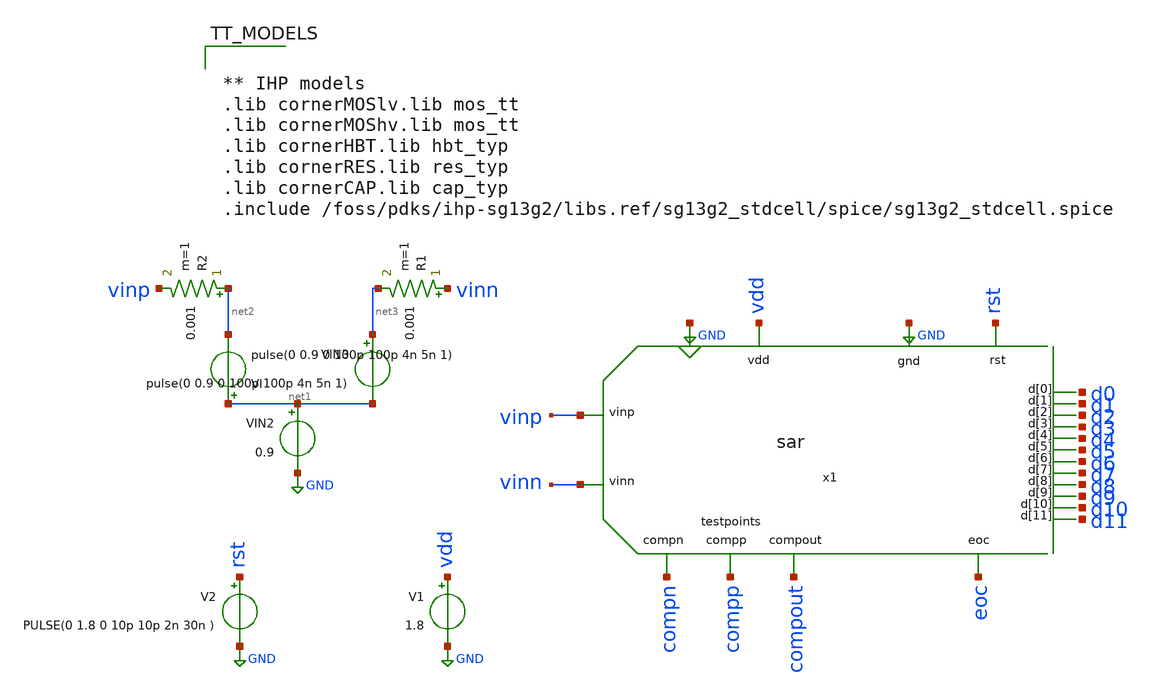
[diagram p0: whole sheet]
** sch_path: xschem/SAR_ADC/testbench/tb_sar_adc.sch
**.subckt tb_sar_adc
x1 vinp rst GND vinn GND vdd compn compp compout eoc d9 d7 d0 d11 d3 d4 d2 d1 d8 d6 d5 d10 sar
VI net1 net2 pulse(0 0.9 0 100p 100p 4n 5n 1)
V1 vdd GND 1.8
VIN2 net1 GND 0.9
VIN3 net3 net1 pulse(0 0.9 0 100p 100p 4n 5n 1)
V2 rst GND PULSE(0 1.8 0 10p 10p 2n 30n )
R2 net2 vinp 0.001 m=1
R1 vinn net3 0.001 m=1
**** begin user architecture code


.param periodclk=1n
.param periodconv=30n
.param stoptime=1*periodconv
.param ro = 300

.param W_P = 1.0u
.param L_P = 0.13u
.param W_N = 1.0u
.param L_N = 0.13u

.options klu method=gear reltol=1e-2 abstol=1e-15 gmin=1e-15


.tran {0.01*periodclk} {stoptime}

.control

run

plot {(V(d11)*2+V(d10)*4+V(d9)*8+V(d8)*16+V(d7)*32+V(d6)*64+V(d5)*128+V(d4)*256+V(d3)*512+V(d2)*1024+V(d1)*2048)/4096}
+ {2*rst} eoc {vinp - vinn}
plot {(V(d11)*2+V(d10)*4+V(d9)*8+V(d8)*16+V(d7)*32+V(d6)*64+V(d5)*128+V(d4)*256+V(d3)*512+V(d2)*1024+V(d1)*2048-V(d0)*4096)/4096}
+ {2*rst} eoc {vinp - vinn}
plot {(-V(d0)*2048 + V(d1)*1024 + V(d2)*512 + V(d3)*256 + V(d4)*128 + V(d5)*64 + V(d6)*32 + V(d7)*16 + V(d8)*8 + V(d9)*4 + V(d10)*2 + V(d11))/2048}
plot {((V(d0)-1.8)*2048 + V(d1)*1024 + V(d2)*512 + V(d3)*256 + V(d4)*128 + V(d5)*64 + V(d6)*32 + V(d7)*16 + V(d8)*8 + V(d9)*4 + V(d10)*2 + V(d11))/2048}
+ rst eoc vinp-vinn
plot compp compn {compout + 4}
plot {d0} {d1 + 4} {d2 + 8} {d3 + 12} {d4 + 16} {d5 + 20} {d6 + 24} {d7 + 28} {d8 + 32} {d9 + 36} {d10 + 40}
+ {d11 + 44} {x1.comp_clk + 50} {compout + 55} {eoc + 60}  {compp - compn - 2}
plot compp-compn x1.comp_clk compout

*wrdata adc_signals.csv time V(d0) V(d1) V(d2) V(d3) V(d4) V(d5) V(d6) V(d7) V(d8) V(d9) V(d10)
*+ V(d11) vinp vinn eoc rst compout compp compn x1.comp_clk
*write adc_signals.raw time V(d0) V(d1) V(d2) V(d3) V(d4) V(d5) V(d6) V(d7) V(d8) V(d9) V(d10)
*+ V(d11) vinp vinn eoc rst compout compp compn x1.comp_clk
*quit
.endc




** IHP models
.lib cornerMOSlv.lib mos_tt
.lib cornerMOShv.lib mos_tt
.lib cornerHBT.lib hbt_typ
.lib cornerRES.lib res_typ
.lib cornerCAP.lib cap_typ
.include /foss/pdks/ihp-sg13g2/libs.ref/sg13g2_stdcell/spice/sg13g2_stdcell.spice


**** end user architecture code
**.ends
.GLOBAL GND
.end
